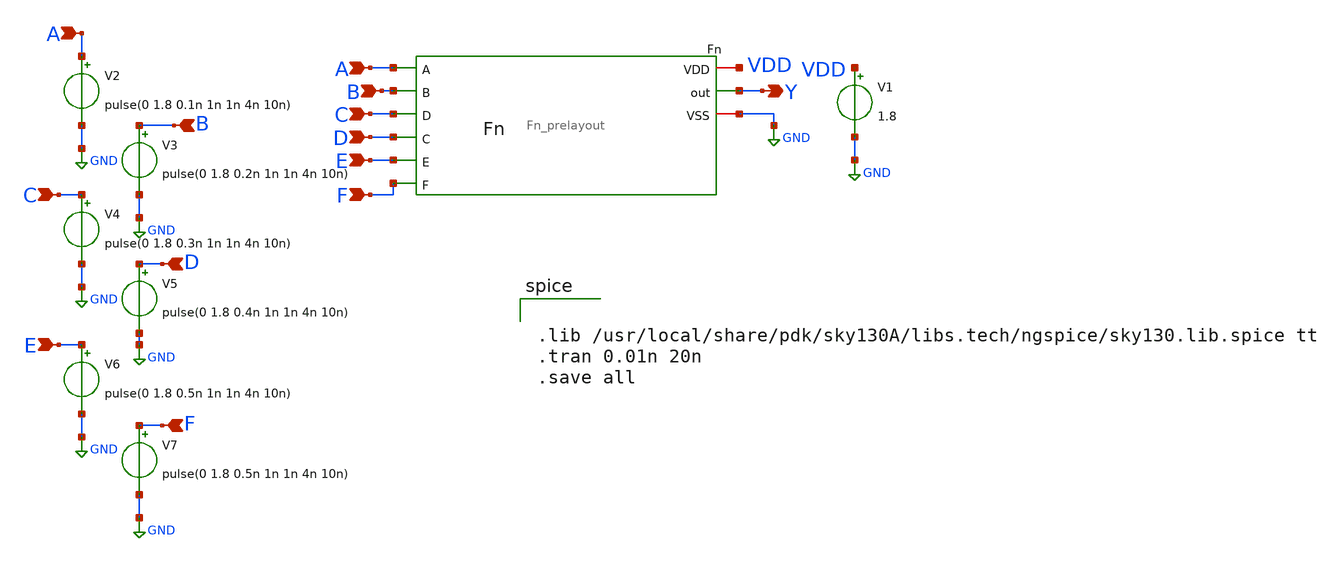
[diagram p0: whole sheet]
** sch_path: week2/Fn/Fn_prelayout_tb.sch
**.subckt Fn_prelayout_tb Y A A B C D E F B C D E F
*.opin Y
*.ipin A
*.ipin A
*.ipin B
*.ipin C
*.ipin D
*.ipin E
*.ipin F
*.ipin B
*.ipin C
*.ipin D
*.ipin E
*.ipin F
x1 VDD A B C D E F Y GND Fn_prelayout
V1 VDD GND 1.8
V2 A GND pulse(0 1.8 0.1n 1n 1n 4n 10n)
V3 B GND pulse(0 1.8 0.2n 1n 1n 4n 10n)
V4 C GND pulse(0 1.8 0.3n 1n 1n 4n 10n)
V5 D GND pulse(0 1.8 0.4n 1n 1n 4n 10n)
V6 E GND pulse(0 1.8 0.5n 1n 1n 4n 10n)
V7 F GND pulse(0 1.8 0.5n 1n 1n 4n 10n)
**** begin user architecture code


.lib /usr/local/share/pdk/sky130A/libs.tech/ngspice/sky130.lib.spice tt
.tran 0.01n 20n
.save all

**** end user architecture code
**.ends

* expanding   symbol:  Fn_prelayout.sym # of pins=9
** sym_path: week2/Fn/Fn_prelayout.sym
** sch_path: week2/Fn/Fn_prelayout.sch
.subckt Fn_prelayout VDD A B D C E F out VSS
*.ipin A
*.ipin B
*.ipin C
*.ipin D
*.ipin E
*.ipin F
*.opin out
*.iopin VDD
*.iopin VSS
XM1 net1 A VDD VDD sky130_fd_pr__pfet_01v8 L=0.15 W=1 nf=1 ad='int((nf+1)/2) * W/nf * 0.29' as='int((nf+2)/2) * W/nf * 0.29'
+ pd='2*int((nf+1)/2) * (W/nf + 0.29)' ps='2*int((nf+2)/2) * (W/nf + 0.29)' nrd='0.29 / W' nrs='0.29 / W'
+ sa=0 sb=0 sd=0 mult=1 m=1
XM2 net3 B VDD VDD sky130_fd_pr__pfet_01v8 L=0.15 W=1 nf=1 ad='int((nf+1)/2) * W/nf * 0.29' as='int((nf+2)/2) * W/nf * 0.29'
+ pd='2*int((nf+1)/2) * (W/nf + 0.29)' ps='2*int((nf+2)/2) * (W/nf + 0.29)' nrd='0.29 / W' nrs='0.29 / W'
+ sa=0 sb=0 sd=0 mult=1 m=1
XM3 net2 C net1 net1 sky130_fd_pr__pfet_01v8 L=0.15 W=1 nf=1 ad='int((nf+1)/2) * W/nf * 0.29' as='int((nf+2)/2) * W/nf * 0.29'
+ pd='2*int((nf+1)/2) * (W/nf + 0.29)' ps='2*int((nf+2)/2) * (W/nf + 0.29)' nrd='0.29 / W' nrs='0.29 / W'
+ sa=0 sb=0 sd=0 mult=1 m=1
XM4 net2 D net3 net3 sky130_fd_pr__pfet_01v8 L=0.15 W=1 nf=1 ad='int((nf+1)/2) * W/nf * 0.29' as='int((nf+2)/2) * W/nf * 0.29'
+ pd='2*int((nf+1)/2) * (W/nf + 0.29)' ps='2*int((nf+2)/2) * (W/nf + 0.29)' nrd='0.29 / W' nrs='0.29 / W'
+ sa=0 sb=0 sd=0 mult=1 m=1
XM5 out E net2 net2 sky130_fd_pr__pfet_01v8 L=0.15 W=1 nf=1 ad='int((nf+1)/2) * W/nf * 0.29' as='int((nf+2)/2) * W/nf * 0.29'
+ pd='2*int((nf+1)/2) * (W/nf + 0.29)' ps='2*int((nf+2)/2) * (W/nf + 0.29)' nrd='0.29 / W' nrs='0.29 / W'
+ sa=0 sb=0 sd=0 mult=1 m=1
XM6 out F net2 net2 sky130_fd_pr__pfet_01v8 L=0.15 W=1 nf=1 ad='int((nf+1)/2) * W/nf * 0.29' as='int((nf+2)/2) * W/nf * 0.29'
+ pd='2*int((nf+1)/2) * (W/nf + 0.29)' ps='2*int((nf+2)/2) * (W/nf + 0.29)' nrd='0.29 / W' nrs='0.29 / W'
+ sa=0 sb=0 sd=0 mult=1 m=1
XM7 out A net4 net4 sky130_fd_pr__nfet_01v8 L=0.15 W=1 nf=1 ad='int((nf+1)/2) * W/nf * 0.29' as='int((nf+2)/2) * W/nf * 0.29'
+ pd='2*int((nf+1)/2) * (W/nf + 0.29)' ps='2*int((nf+2)/2) * (W/nf + 0.29)' nrd='0.29 / W' nrs='0.29 / W'
+ sa=0 sb=0 sd=0 mult=1 m=1
XM8 out C net4 net4 sky130_fd_pr__nfet_01v8 L=0.15 W=1 nf=1 ad='int((nf+1)/2) * W/nf * 0.29' as='int((nf+2)/2) * W/nf * 0.29'
+ pd='2*int((nf+1)/2) * (W/nf + 0.29)' ps='2*int((nf+2)/2) * (W/nf + 0.29)' nrd='0.29 / W' nrs='0.29 / W'
+ sa=0 sb=0 sd=0 mult=1 m=1
XM9 net4 B VSS VSS sky130_fd_pr__nfet_01v8 L=0.15 W=1 nf=1 ad='int((nf+1)/2) * W/nf * 0.29' as='int((nf+2)/2) * W/nf * 0.29'
+ pd='2*int((nf+1)/2) * (W/nf + 0.29)' ps='2*int((nf+2)/2) * (W/nf + 0.29)' nrd='0.29 / W' nrs='0.29 / W'
+ sa=0 sb=0 sd=0 mult=1 m=1
XM10 net4 D VSS VSS sky130_fd_pr__nfet_01v8 L=0.15 W=1 nf=1 ad='int((nf+1)/2) * W/nf * 0.29' as='int((nf+2)/2) * W/nf * 0.29'
+ pd='2*int((nf+1)/2) * (W/nf + 0.29)' ps='2*int((nf+2)/2) * (W/nf + 0.29)' nrd='0.29 / W' nrs='0.29 / W'
+ sa=0 sb=0 sd=0 mult=1 m=1
XM11 out E net5 net5 sky130_fd_pr__nfet_01v8 L=0.15 W=1 nf=1 ad='int((nf+1)/2) * W/nf * 0.29' as='int((nf+2)/2) * W/nf * 0.29'
+ pd='2*int((nf+1)/2) * (W/nf + 0.29)' ps='2*int((nf+2)/2) * (W/nf + 0.29)' nrd='0.29 / W' nrs='0.29 / W'
+ sa=0 sb=0 sd=0 mult=1 m=1
XM12 net5 F VSS VSS sky130_fd_pr__nfet_01v8 L=0.15 W=1 nf=1 ad='int((nf+1)/2) * W/nf * 0.29' as='int((nf+2)/2) * W/nf * 0.29'
+ pd='2*int((nf+1)/2) * (W/nf + 0.29)' ps='2*int((nf+2)/2) * (W/nf + 0.29)' nrd='0.29 / W' nrs='0.29 / W'
+ sa=0 sb=0 sd=0 mult=1 m=1
.ends

.GLOBAL GND
.end
